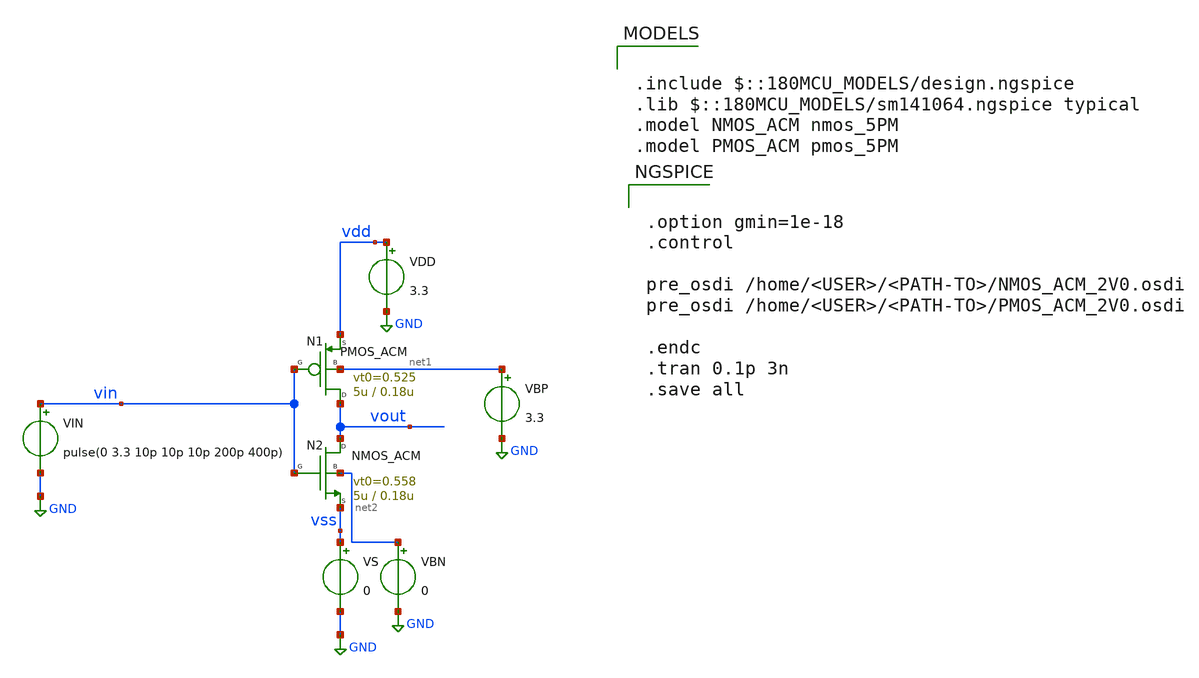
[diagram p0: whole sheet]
** sch_path: legacy/Examples/SkyWater130/xschem/TB_inv_acm.sch
**.subckt TB_inv_acm
N2 vout vin vss net2 NMOS_ACM w=5u l=0.18u n=1.37 is=5.52u vt0=0.558 sigma=27m zeta=56m
VIN vin GND pulse(0 3.3 10p 10p 10p 200p 400p)
VDD vdd GND 3.3
VS vss GND 0
VBP net1 GND 3.3
VBN net2 GND 0
N1 vout vin vdd net1 PMOS_ACM w=5u l=0.18u n=1.40 is=1.82u vt0=0.525 sigma=24m zeta=35m
**** begin user architecture code

.include $::180MCU_MODELS/design.ngspice
.lib $::180MCU_MODELS/sm141064.ngspice typical
.model NMOS_ACM nmos_5PM
.model PMOS_ACM pmos_5PM



.option gmin=1e-18
.control

pre_osdi /home/<USER>/<PATH-TO>/NMOS_ACM_2V0.osdi
pre_osdi /home/<USER>/<PATH-TO>/PMOS_ACM_2V0.osdi

.endc
.tran 0.1p 3n
.save all


**** end user architecture code
**.ends
.GLOBAL GND
.end
